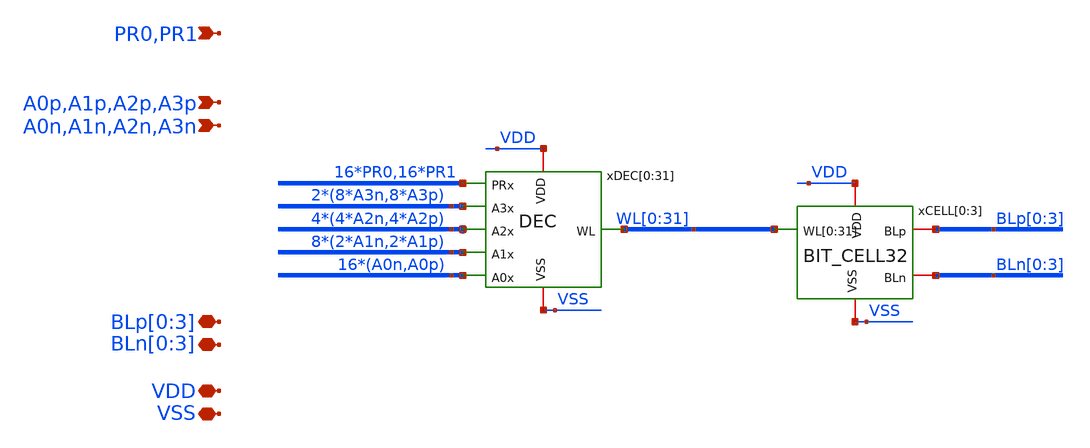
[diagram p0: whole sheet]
** sch_path: module/SRAM128/schematic/SRAM_32x4.sch
**.subckt SRAM_32x4 PR0,PR1 BLn[0],BLn[1],BLn[2],BLn[3] BLp[0],BLp[1],BLp[2],BLp[3] A0n,A1n,A2n,A3n
*+ A0p,A1p,A2p,A3p VSS VDD
*.ipin PR0,PR1
*.iopin BLn[0],BLn[1],BLn[2],BLn[3]
*.iopin BLp[0],BLp[1],BLp[2],BLp[3]
*.ipin A0n,A1n,A2n,A3n
*.ipin A0p,A1p,A2p,A3p
*.iopin VSS
*.iopin VDD
xCELL[0] WL[0] WL[1] WL[2] WL[3] WL[4] WL[5] WL[6] WL[7] WL[8] WL[9] WL[10] WL[11] WL[12] WL[13]
+ WL[14] WL[15] WL[16] WL[17] WL[18] WL[19] WL[20] WL[21] WL[22] WL[23] WL[24] WL[25] WL[26] WL[27] WL[28]
+ WL[29] WL[30] WL[31] BLp[0] BLn[0] VDD VSS BIT_CELL32
xCELL[1] WL[0] WL[1] WL[2] WL[3] WL[4] WL[5] WL[6] WL[7] WL[8] WL[9] WL[10] WL[11] WL[12] WL[13]
+ WL[14] WL[15] WL[16] WL[17] WL[18] WL[19] WL[20] WL[21] WL[22] WL[23] WL[24] WL[25] WL[26] WL[27] WL[28]
+ WL[29] WL[30] WL[31] BLp[1] BLn[1] VDD VSS BIT_CELL32
xCELL[2] WL[0] WL[1] WL[2] WL[3] WL[4] WL[5] WL[6] WL[7] WL[8] WL[9] WL[10] WL[11] WL[12] WL[13]
+ WL[14] WL[15] WL[16] WL[17] WL[18] WL[19] WL[20] WL[21] WL[22] WL[23] WL[24] WL[25] WL[26] WL[27] WL[28]
+ WL[29] WL[30] WL[31] BLp[2] BLn[2] VDD VSS BIT_CELL32
xCELL[3] WL[0] WL[1] WL[2] WL[3] WL[4] WL[5] WL[6] WL[7] WL[8] WL[9] WL[10] WL[11] WL[12] WL[13]
+ WL[14] WL[15] WL[16] WL[17] WL[18] WL[19] WL[20] WL[21] WL[22] WL[23] WL[24] WL[25] WL[26] WL[27] WL[28]
+ WL[29] WL[30] WL[31] BLp[3] BLn[3] VDD VSS BIT_CELL32
xDEC[0] VDD PR0 WL[0] A2n A1n A0n VSS A3n DEC
xDEC[1] VDD PR0 WL[1] A2n A1n A0p VSS A3n DEC
xDEC[2] VDD PR0 WL[2] A2n A1p A0n VSS A3n DEC
xDEC[3] VDD PR0 WL[3] A2n A1p A0p VSS A3n DEC
xDEC[4] VDD PR0 WL[4] A2p A1n A0n VSS A3n DEC
xDEC[5] VDD PR0 WL[5] A2p A1n A0p VSS A3n DEC
xDEC[6] VDD PR0 WL[6] A2p A1p A0n VSS A3n DEC
xDEC[7] VDD PR0 WL[7] A2p A1p A0p VSS A3n DEC
xDEC[8] VDD PR0 WL[8] A2n A1n A0n VSS A3p DEC
xDEC[9] VDD PR0 WL[9] A2n A1n A0p VSS A3p DEC
xDEC[10] VDD PR0 WL[10] A2n A1p A0n VSS A3p DEC
xDEC[11] VDD PR0 WL[11] A2n A1p A0p VSS A3p DEC
xDEC[12] VDD PR0 WL[12] A2p A1n A0n VSS A3p DEC
xDEC[13] VDD PR0 WL[13] A2p A1n A0p VSS A3p DEC
xDEC[14] VDD PR0 WL[14] A2p A1p A0n VSS A3p DEC
xDEC[15] VDD PR0 WL[15] A2p A1p A0p VSS A3p DEC
xDEC[16] VDD PR1 WL[16] A2n A1n A0n VSS A3n DEC
xDEC[17] VDD PR1 WL[17] A2n A1n A0p VSS A3n DEC
xDEC[18] VDD PR1 WL[18] A2n A1p A0n VSS A3n DEC
xDEC[19] VDD PR1 WL[19] A2n A1p A0p VSS A3n DEC
xDEC[20] VDD PR1 WL[20] A2p A1n A0n VSS A3n DEC
xDEC[21] VDD PR1 WL[21] A2p A1n A0p VSS A3n DEC
xDEC[22] VDD PR1 WL[22] A2p A1p A0n VSS A3n DEC
xDEC[23] VDD PR1 WL[23] A2p A1p A0p VSS A3n DEC
xDEC[24] VDD PR1 WL[24] A2n A1n A0n VSS A3p DEC
xDEC[25] VDD PR1 WL[25] A2n A1n A0p VSS A3p DEC
xDEC[26] VDD PR1 WL[26] A2n A1p A0n VSS A3p DEC
xDEC[27] VDD PR1 WL[27] A2n A1p A0p VSS A3p DEC
xDEC[28] VDD PR1 WL[28] A2p A1n A0n VSS A3p DEC
xDEC[29] VDD PR1 WL[29] A2p A1n A0p VSS A3p DEC
xDEC[30] VDD PR1 WL[30] A2p A1p A0n VSS A3p DEC
xDEC[31] VDD PR1 WL[31] A2p A1p A0p VSS A3p DEC
**.ends
.end
